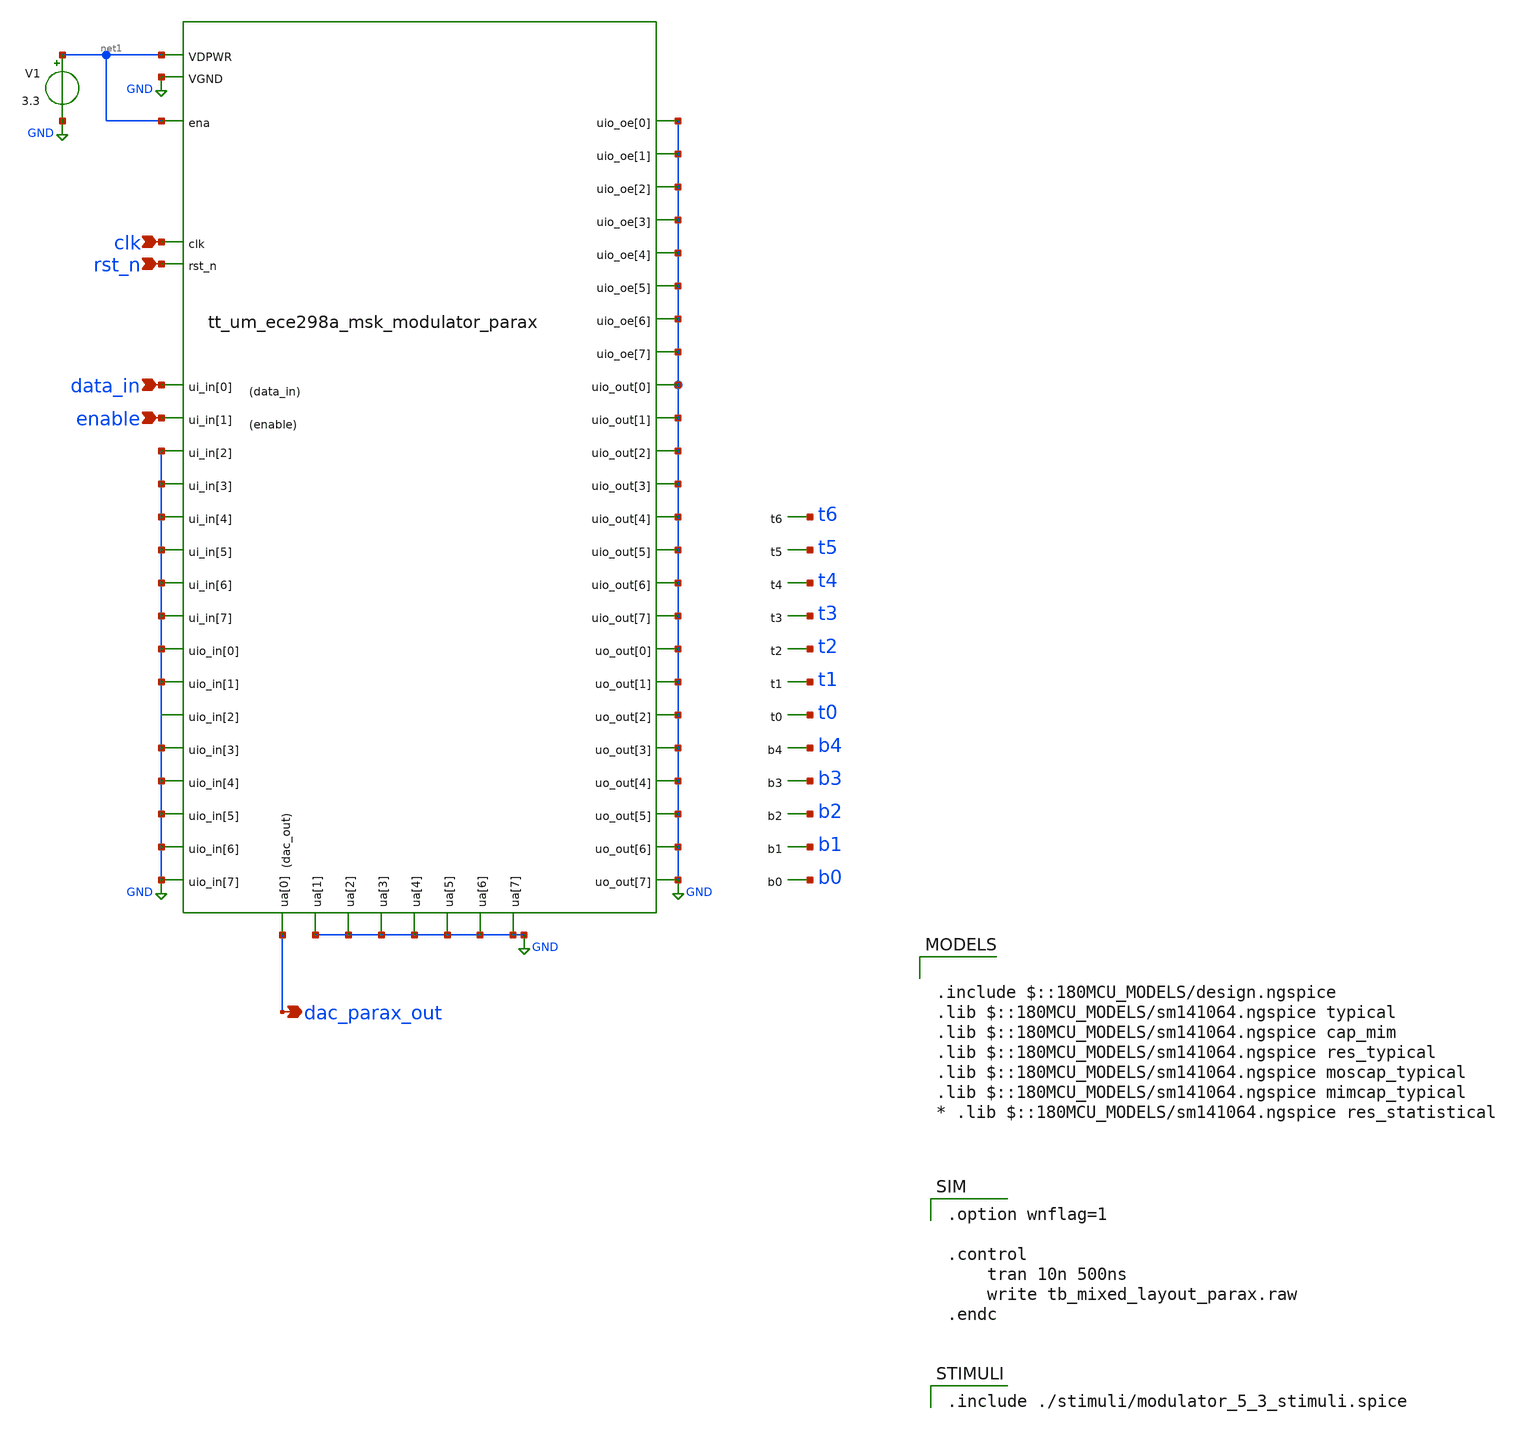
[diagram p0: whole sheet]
** sch_path: xschem/tb_mixed_layout_parax.sch
**.subckt tb_mixed_layout_parax data_in enable clk rst_n dac_parax_out
*.ipin data_in
*.ipin enable
*.ipin clk
*.ipin rst_n
*.opin dac_parax_out
V1 net1 GND 3.3
x1 clk net1 rst_n dac_parax_out GND GND GND GND GND GND GND data_in enable GND GND GND GND GND GND
+ GND GND GND GND GND GND GND GND GND GND GND GND GND GND GND GND GND GND GND GND GND GND GND GND GND GND
+ GND GND GND GND GND GND net1 t6 t5 t4 t3 t2 t1 t0 b4 b3 b2 b1 b0 tt_um_ece298a_msk_modulator_parax
**** begin user architecture code

.option wnflag=1

.control
    tran 10n 500ns
    write tb_mixed_layout_parax.raw
.endc



.include ./stimuli/modulator_5_3_stimuli.spice


.include $::180MCU_MODELS/design.ngspice
.lib $::180MCU_MODELS/sm141064.ngspice typical
.lib $::180MCU_MODELS/sm141064.ngspice cap_mim
.lib $::180MCU_MODELS/sm141064.ngspice res_typical
.lib $::180MCU_MODELS/sm141064.ngspice moscap_typical
.lib $::180MCU_MODELS/sm141064.ngspice mimcap_typical
* .lib $::180MCU_MODELS/sm141064.ngspice res_statistical

**** end user architecture code
**.ends

* expanding   symbol:  tt_um_ece298a_msk_modulator_parax.sym # of pins=64
** sym_path: xschem/tt_um_ece298a_msk_modulator_parax.sym
.include ../../mag/spice/tt_um_ece298a_msk_modulator_parax.spice
.GLOBAL GND
.end
